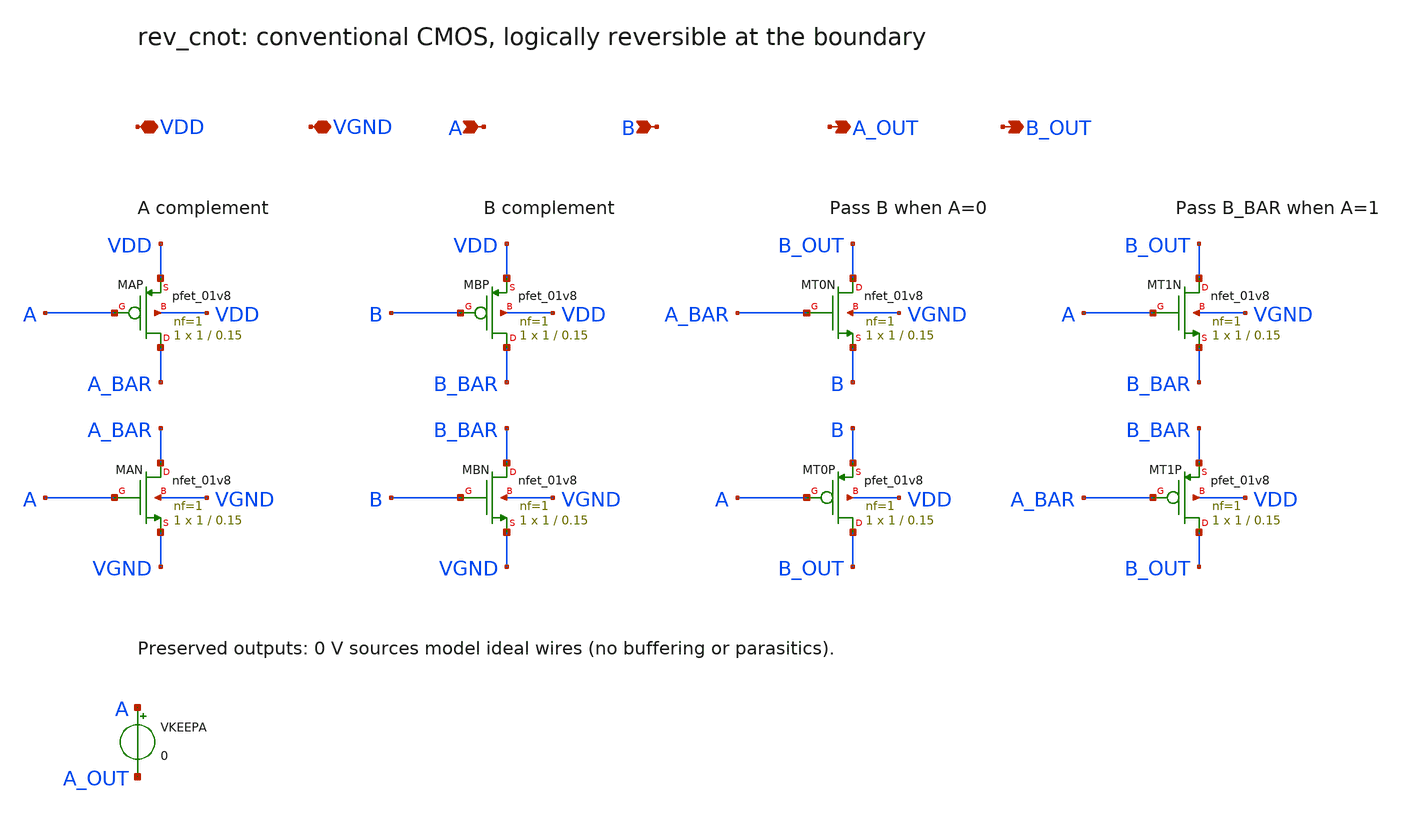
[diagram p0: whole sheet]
** sch_path: src/reversible_stdcells/rev_cnot/rev_cnot.sch
**.subckt rev_cnot VDD VGND A B A_OUT B_OUT
*.iopin VDD
*.iopin VGND
*.ipin A
*.ipin B
*.opin A_OUT
*.opin B_OUT
XMAP A_BAR A VDD VDD sky130_fd_pr__pfet_01v8 L=0.15 W=1 nf=1 ad=0.29 as=0.29 pd=2.58 ps=2.58
+ nrd=0.29 nrs=0.29 sa=0 sb=0 sd=0 mult=1 m=1
XMAN A_BAR A VGND VGND sky130_fd_pr__nfet_01v8 L=0.15 W=1 nf=1 ad=0.29 as=0.29 pd=2.58 ps=2.58
+ nrd=0.29 nrs=0.29 sa=0 sb=0 sd=0 mult=1 m=1
XMBP B_BAR B VDD VDD sky130_fd_pr__pfet_01v8 L=0.15 W=1 nf=1 ad=0.29 as=0.29 pd=2.58 ps=2.58
+ nrd=0.29 nrs=0.29 sa=0 sb=0 sd=0 mult=1 m=1
XMBN B_BAR B VGND VGND sky130_fd_pr__nfet_01v8 L=0.15 W=1 nf=1 ad=0.29 as=0.29 pd=2.58 ps=2.58
+ nrd=0.29 nrs=0.29 sa=0 sb=0 sd=0 mult=1 m=1
XMT0N B_OUT A_BAR B VGND sky130_fd_pr__nfet_01v8 L=0.15 W=1 nf=1 ad=0.29 as=0.29 pd=2.58 ps=2.58
+ nrd=0.29 nrs=0.29 sa=0 sb=0 sd=0 mult=1 m=1
XMT0P B_OUT A B VDD sky130_fd_pr__pfet_01v8 L=0.15 W=1 nf=1 ad=0.29 as=0.29 pd=2.58 ps=2.58 nrd=0.29
+ nrs=0.29 sa=0 sb=0 sd=0 mult=1 m=1
XMT1N B_OUT A B_BAR VGND sky130_fd_pr__nfet_01v8 L=0.15 W=1 nf=1 ad=0.29 as=0.29 pd=2.58 ps=2.58
+ nrd=0.29 nrs=0.29 sa=0 sb=0 sd=0 mult=1 m=1
XMT1P B_OUT A_BAR B_BAR VDD sky130_fd_pr__pfet_01v8 L=0.15 W=1 nf=1 ad=0.29 as=0.29 pd=2.58 ps=2.58
+ nrd=0.29 nrs=0.29 sa=0 sb=0 sd=0 mult=1 m=1
VKEEPA A A_OUT 0
**.ends
.end
